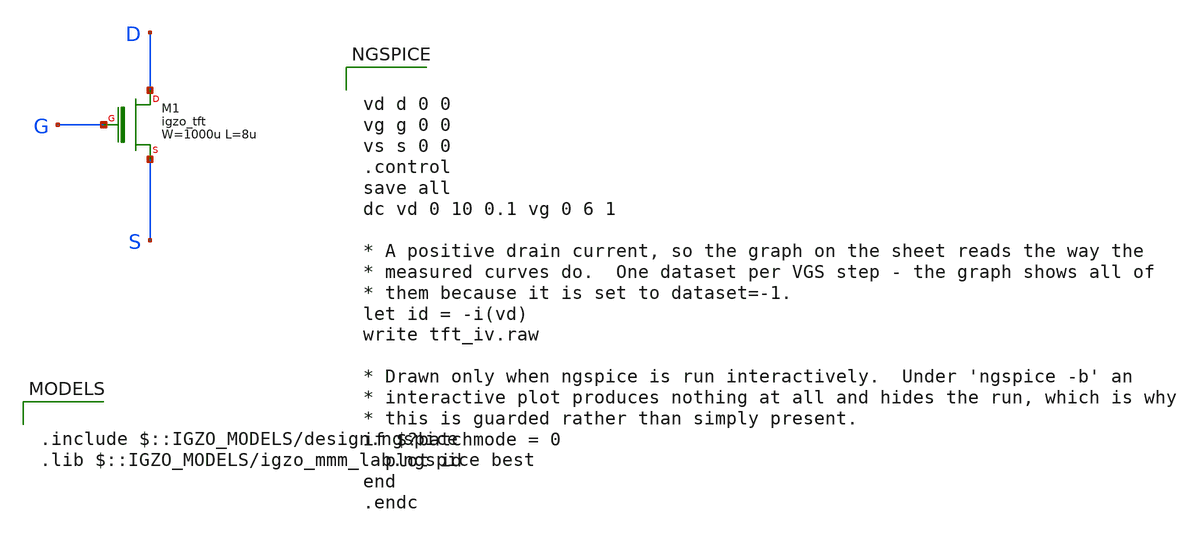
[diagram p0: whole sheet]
** sch_path: libs.tech/xschem/tests/tft_iv.sch
**.subckt tft_iv
XM1 D G S igzo_tft W=1000u L=8u ov=5u nf=1 m=1
**** begin user architecture code

.include $::IGZO_MODELS/design.ngspice
.lib $::IGZO_MODELS/igzo_mmm_lab.ngspice best



vd d 0 0
vg g 0 0
vs s 0 0
.control
save all
dc vd 0 10 0.1 vg 0 6 1

* A positive drain current, so the graph on the sheet reads the way the
* measured curves do.  One dataset per VGS step - the graph shows all of
* them because it is set to dataset=-1.
let id = -i(vd)
write tft_iv.raw

* Drawn only when ngspice is run interactively.  Under 'ngspice -b' an
* interactive plot produces nothing at all and hides the run, which is why
* this is guarded rather than simply present.
if $?batchmode = 0
  plot id
end
.endc


**** end user architecture code
**.ends
.end
